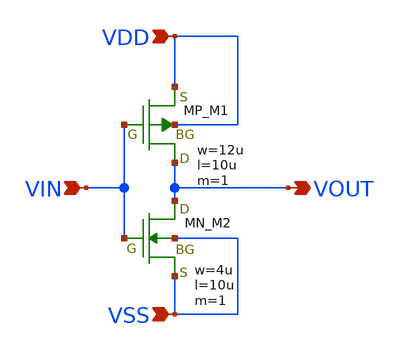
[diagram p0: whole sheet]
** sch_path: member_project/JJY_Receiver/Masahiro/jjy_recv/XTALOSC/XTALOSC_INV.sch
**.subckt XTALOSC_INV VSS VDD VIN VOUT
*.ipin VSS
*.ipin VDD
*.ipin VIN
*.opin VOUT
XM1 VOUT VIN VDD VDD PMOS w=12u l=10u as=0 ad=0 ps=0 pd=0 nrd=0 nrs=0 m=1
XM2 VOUT VIN VSS VSS NMOS w=4u l=10u as=0 ad=0 ps=0 pd=0 nrd=0 nrs=0 m=1
**.ends
.end
